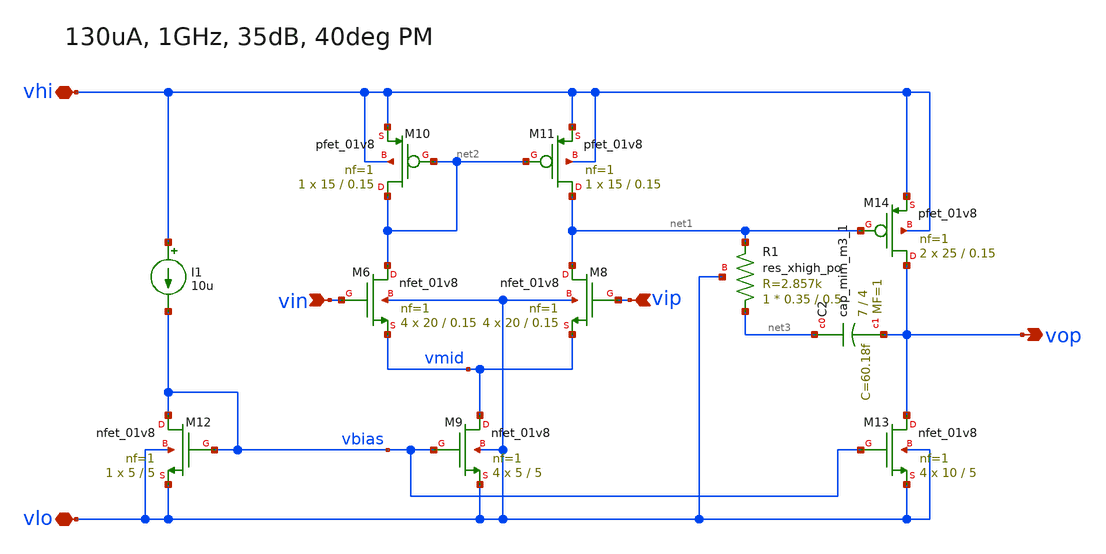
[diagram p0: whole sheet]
** sch_path: xschem/5tamp_2st_model.sch
**.subckt 5tamp_2st_model vip vin vhi vlo vop
*.ipin vip
*.ipin vin
*.iopin vhi
*.iopin vlo
*.opin vop
XM6 net2 vin vmid vlo sky130_fd_pr__nfet_01v8 L=0.15 W=20 nf=1 ad='int((nf+1)/2) * W/nf * 0.29' as='int((nf+2)/2) * W/nf * 0.29'
+ pd='2*int((nf+1)/2) * (W/nf + 0.29)' ps='2*int((nf+2)/2) * (W/nf + 0.29)' nrd='0.29 / W' nrs='0.29 / W'
+ sa=0 sb=0 sd=0 mult=4 m=4
XM8 net1 vip vmid vlo sky130_fd_pr__nfet_01v8 L=0.15 W=20 nf=1 ad='int((nf+1)/2) * W/nf * 0.29' as='int((nf+2)/2) * W/nf * 0.29'
+ pd='2*int((nf+1)/2) * (W/nf + 0.29)' ps='2*int((nf+2)/2) * (W/nf + 0.29)' nrd='0.29 / W' nrs='0.29 / W'
+ sa=0 sb=0 sd=0 mult=4 m=4
XM9 vmid vbias vlo vlo sky130_fd_pr__nfet_01v8 L=5 W=5 nf=1 ad='int((nf+1)/2) * W/nf * 0.29' as='int((nf+2)/2) * W/nf * 0.29'
+ pd='2*int((nf+1)/2) * (W/nf + 0.29)' ps='2*int((nf+2)/2) * (W/nf + 0.29)' nrd='0.29 / W' nrs='0.29 / W'
+ sa=0 sb=0 sd=0 mult=4 m=4
XM10 net2 net2 vhi vhi sky130_fd_pr__pfet_01v8 L=0.15 W=15 nf=1 ad='int((nf+1)/2) * W/nf * 0.29' as='int((nf+2)/2) * W/nf * 0.29'
+ pd='2*int((nf+1)/2) * (W/nf + 0.29)' ps='2*int((nf+2)/2) * (W/nf + 0.29)' nrd='0.29 / W' nrs='0.29 / W'
+ sa=0 sb=0 sd=0 mult=1 m=1
XM11 net1 net2 vhi vhi sky130_fd_pr__pfet_01v8 L=0.15 W=15 nf=1 ad='int((nf+1)/2) * W/nf * 0.29' as='int((nf+2)/2) * W/nf * 0.29'
+ pd='2*int((nf+1)/2) * (W/nf + 0.29)' ps='2*int((nf+2)/2) * (W/nf + 0.29)' nrd='0.29 / W' nrs='0.29 / W'
+ sa=0 sb=0 sd=0 mult=1 m=1
I1 vhi vbias 10u
XM12 vbias vbias vlo vlo sky130_fd_pr__nfet_01v8 L=5 W=5 nf=1 ad='int((nf+1)/2) * W/nf * 0.29' as='int((nf+2)/2) * W/nf * 0.29'
+ pd='2*int((nf+1)/2) * (W/nf + 0.29)' ps='2*int((nf+2)/2) * (W/nf + 0.29)' nrd='0.29 / W' nrs='0.29 / W'
+ sa=0 sb=0 sd=0 mult=1 m=1
XM13 vop vbias vlo vlo sky130_fd_pr__nfet_01v8 L=5 W=10 nf=1 ad='int((nf+1)/2) * W/nf * 0.29' as='int((nf+2)/2) * W/nf * 0.29'
+ pd='2*int((nf+1)/2) * (W/nf + 0.29)' ps='2*int((nf+2)/2) * (W/nf + 0.29)' nrd='0.29 / W' nrs='0.29 / W'
+ sa=0 sb=0 sd=0 mult=4 m=4
XM14 vop net1 vhi vhi sky130_fd_pr__pfet_01v8 L=0.15 W=25 nf=1 ad='int((nf+1)/2) * W/nf * 0.29' as='int((nf+2)/2) * W/nf * 0.29'
+ pd='2*int((nf+1)/2) * (W/nf + 0.29)' ps='2*int((nf+2)/2) * (W/nf + 0.29)' nrd='0.29 / W' nrs='0.29 / W'
+ sa=0 sb=0 sd=0 mult=2 m=2
XR1 net3 net1 vlo sky130_fd_pr__res_xhigh_po W=0.35 L=0.5 mult=1 m=1
XC2 net3 vop sky130_fd_pr__cap_mim_m3_1 W=7 L=4 MF=1 m=1
**.ends
.end
